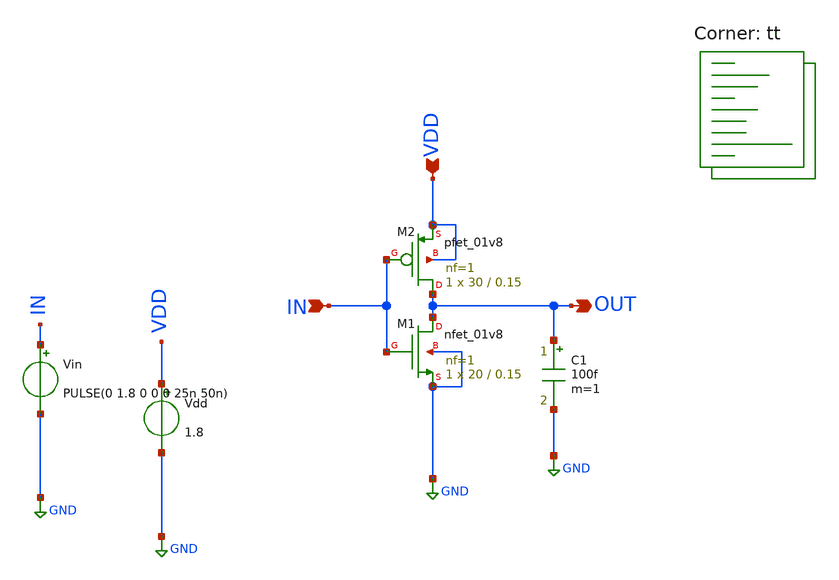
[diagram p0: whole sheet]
** sch_path: sizing-inverter.sch
**.subckt sizing-inverter IN VDD OUT
*.ipin IN
*.ipin VDD
*.opin OUT
Vin IN GND PULSE(0 1.8 0 0 0 25n 50n)
Vdd VDD GND 1.8
XM1 OUT IN GND GND sky130_fd_pr__nfet_01v8 L=0.15 W=20 nf=1 ad='int((nf+1)/2) * W/nf * 0.29' as='int((nf+2)/2) * W/nf * 0.29'
+ pd='2*int((nf+1)/2) * (W/nf + 0.29)' ps='2*int((nf+2)/2) * (W/nf + 0.29)' nrd='0.29 / W' nrs='0.29 / W'
+ sa=0 sb=0 sd=0 mult=1 m=1
XM2 OUT IN VDD VDD sky130_fd_pr__pfet_01v8 L=0.15 W=30 nf=1 ad='int((nf+1)/2) * W/nf * 0.29' as='int((nf+2)/2) * W/nf * 0.29'
+ pd='2*int((nf+1)/2) * (W/nf + 0.29)' ps='2*int((nf+2)/2) * (W/nf + 0.29)' nrd='0.29 / W' nrs='0.29 / W'
+ sa=0 sb=0 sd=0 mult=1 m=1
C1 OUT GND 100f m=1
**** begin user architecture code
.lib $::SKYWATER_MODELS/sky130.lib.spice tt


.options savecurrents

.control
save all

let step=1
let max_w=80
let curr_w=10

let min_diff=100
let best_w=curr_w

let iters = ceil((max_w - curr_w)/step)
let iter = 0

let switching_points = vector(iters)
let diffs = vector(iters)
let width = vector(iters)


while curr_w < max_w

	alter m.xm2.msky130_fd_pr__pfet_01v8 W=curr_w

	tran 10p 50n
	meas tran rise_time TRIG v(out) VAL=0.1 RISE=1 TARG v(out) VAL=1.62 RISE=1
	meas tran fall_time TRIG v(out) VAL=1.62 FALL=1 TARG v(out) VAL=0.1 FALL=1

	let diffs[iter] = abs( $&rise_time - $&fall_time )


	dc vin 0 1.8 1m

	meas dc switching_point WHEN v(out)=v(in) CROSS=LAST
	set plotstr = ( $plotstr {$curplot}.v(out) )
	set global_switching_point = $&switching_point

	let difference=abs($&switching_point - 0.9)

	if difference < min_diff
		let best_w = curr_w
		let min_diff = difference
	end


	let switching_points[iter] = $&switching_point
	let width[iter] = curr_w



	let curr_w=curr_w + step
	let iter=iter + 1

	end
set plotstr = ( $plotstr {$curplot}.v(in) )

set nolegend

plot switching_points vs width title 'switching points vs time' xlabel 'width' ylabel 'Switching point (V)'
plot diffs vs width title 'asymmetricity vs time' xlabel 'width' ylabel 'Difference in rise/fall'

plot $plotstr

.endc


**** end user architecture code
**.ends
.GLOBAL GND
.end
